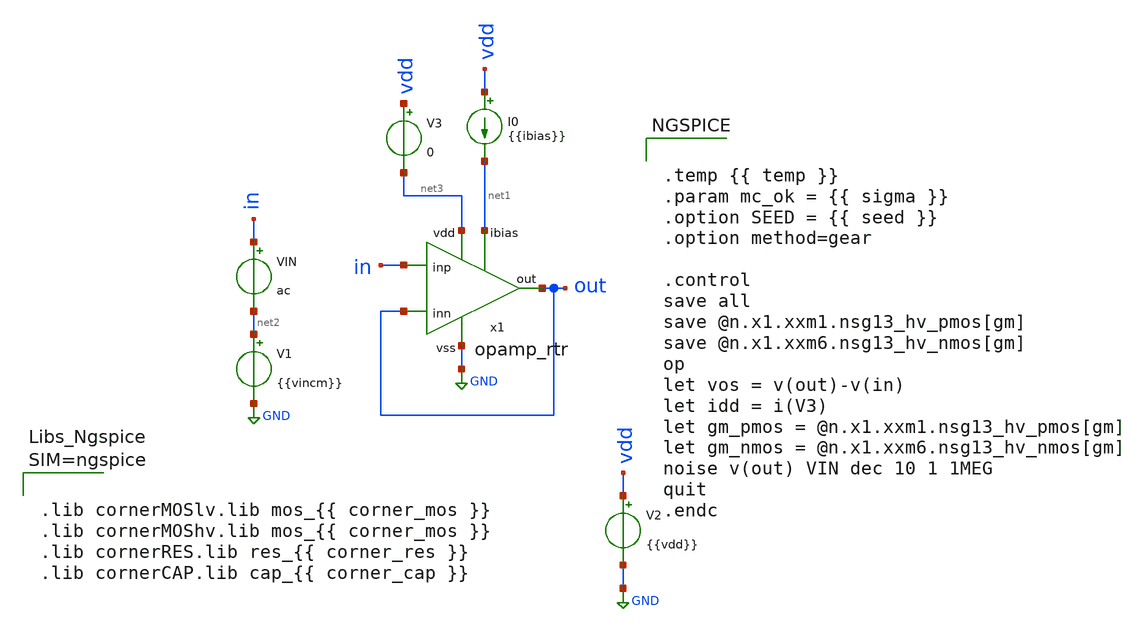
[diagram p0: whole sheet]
** sch_path: testbenches/xschem/tb_opamp_rtr_op.sch
**.subckt tb_opamp_rtr_op
V1 net2 GND {{vincm}}
.save i(v1)
V2 vdd GND {{vdd}}
I0 vdd net1 {{ibias}}
V3 vdd net3 0
.save i(v3)
VIN in net2 ac
.save i(vin)
x1 net3 in GND out net1 out opamp_rtr
**** begin user architecture code


.temp {{ temp }}
.param mc_ok = {{ sigma }}
.option SEED = {{ seed }}
.option method=gear

.control
save all
save @n.x1.xxm1.nsg13_hv_pmos[gm]
save @n.x1.xxm6.nsg13_hv_nmos[gm]
op
let vos = v(out)-v(in)
let idd = i(V3)
let gm_pmos = @n.x1.xxm1.nsg13_hv_pmos[gm]
let gm_nmos = @n.x1.xxm6.nsg13_hv_nmos[gm]
noise v(out) VIN dec 10 1 1MEG
quit
.endc





.lib cornerMOSlv.lib mos_{{ corner_mos }}
.lib cornerMOShv.lib mos_{{ corner_mos }}
.lib cornerRES.lib res_{{ corner_res }}
.lib cornerCAP.lib cap_{{ corner_cap }}



**** end user architecture code
**.ends

* expanding   symbol:  heichip/opamp_rtr/schematic/xschem/opamp_rtr.sym # of pins=6
** sym_path: schematic/xschem/opamp_rtr.sym
** sch_path: schematic/xschem/opamp_rtr.sch
.subckt opamp_rtr vdd inp vss inn ibias out
*.ipin inp
*.opin out
*.iopin vdd
*.ipin inn
*.ipin ibias
*.iopin vss
XXM6 out1_n inp ncmdiff_n vss sg13_hv_nmos w={w_diff_n} l={l_diff} ng={n_diff_n} m=1 mm_ok=1
XXM1 net1 inn ncmdiff_p vdd sg13_hv_pmos w={w_diff_p} l={l_diff} ng={n_diff_p} m=1 mm_ok=1
XXM2 ncmdiff_p inp out1_p vdd sg13_hv_pmos w={w_diff_p} l={l_diff} ng={n_diff_p} m=1 mm_ok=1
XXM3 ncmdiff_p vbias_p vdd vdd sg13_hv_pmos w={w_tail_p} l={l_bias} ng={n_tail_p} m=1 mm_ok=1
XXM4 vss net1 net1 vss sg13_hv_nmos w={w_load_n} l={l_load} ng={n_load_n} m=1 mm_ok=1
XXM5 out1_p net1 vss vss sg13_hv_nmos w={w_load_n} l={l_load} ng={n_load_n} m=1 mm_ok=1
XXM7 ncmdiff_n inn net2 vss sg13_hv_nmos w={w_diff_n} l={l_diff} ng={n_diff_n} m=1 mm_ok=1
XXM8 ncmdiff_n ibias vss vss sg13_hv_nmos w={w_tail_n} l={l_bias} ng={n_tail_n} m=1 mm_ok=1
XXM9 vdd net2 out1_n vdd sg13_hv_pmos w={w_load_p} l={l_load} ng={n_load_p} m=1 mm_ok=1
XXM10 net2 net2 vdd vdd sg13_hv_pmos w={w_load_p} l={l_load} ng={n_load_p} m=1 mm_ok=1
XXM25 nswa vref_p ncmdiff_p ncmdiff_p sg13_hv_pmos w={w_sw_p} l={l_sw} ng={n_sw_p} m=1 mm_ok=1
XXM26 nswa nswa vss vss sg13_hv_nmos w={w_gmn} l={l_bias} ng={n_gmn} m=1 mm_ok=1
XXM27 ncmdiff_n nswa vss vss sg13_hv_nmos w={w_gmn} l={l_bias} ng={n_gmn} m=1 mm_ok=1
XXM28 ncmdiff_n vref_n nswb vss sg13_hv_nmos w={w_sw_n} l={l_sw} ng={n_sw_n} m=1 mm_ok=1
XXM29 nswb nswb vdd vdd sg13_hv_pmos w={w_gmp} l={l_bias} ng={n_gmp} m=1 mm_ok=1
XXM30 ncmdiff_p nswb vdd vdd sg13_hv_pmos w={w_gmp} l={l_bias} ng={n_gmp} m=1 mm_ok=1
XXM13 out1_n nabn out1_p vss sg13_hv_nmos w={w_ab_n} l={l_ab} ng={n_ab_n} m=1 mm_ok=1
XXM14 out1_p nabp out1_n vdd sg13_hv_pmos w={w_ab_p} l={l_ab} ng={n_ab_p} m=1 mm_ok=1
XXM15 out1_n vbias_p vdd vdd sg13_hv_pmos w={w_ab_src} l={l_bias} ng={n_ab_src} m=1 mm_ok=1
XXM16 out1_p nab_ref vss vss sg13_hv_nmos w={w_ab_snk} l={l_bias} ng={n_ab_snk} m=1 mm_ok=1
XXM23 nab_ref vbias_p vdd vdd sg13_hv_pmos w={w_ab_src} l={l_bias} ng={n_ab_src} m=1 mm_ok=1
XXM24 nab_ref nab_ref vss vss sg13_hv_nmos w={w_ab_snk} l={l_bias} ng={n_ab_snk} m=1 mm_ok=1
XXM17 nabn vbias_p vdd vdd sg13_hv_pmos w={w_ab_src} l={l_bias} ng={n_ab_src} m=1 mm_ok=1
XXM18 nabn nabn net3 vss sg13_hv_nmos w={w_ab_n} l={l_ab} ng={n_ab_n} m=1 mm_ok=1
XXM19 net3 net3 vss vss sg13_hv_nmos w={w_ab_n} l={l_ab} ng={n_ab_n} m=1 mm_ok=1
XXM20 nabp nab_ref vss vss sg13_hv_nmos w={w_ab_snk} l={l_bias} ng={n_ab_snk} m=1 mm_ok=1
XXM21 nabp nabp net4 vdd sg13_hv_pmos w={w_ab_p} l={l_ab} ng={n_ab_p} m=1 mm_ok=1
XXM22 net4 net4 vdd vdd sg13_hv_pmos w={w_ab_p} l={l_ab} ng={n_ab_p} m=1 mm_ok=1
XXM11 out out1_n vdd vdd sg13_hv_pmos w={w_out_p} l={l_out} ng={n_out_p} m=1 mm_ok=1
XXM12 out out1_p vss vss sg13_hv_nmos w={w_out_n} l={l_out} ng={n_out_n} m=1 mm_ok=1
XXB1 ibias ibias vss vss sg13_hv_nmos w={w_bias_n} l={l_bias} ng={n_bias_n} m=1 mm_ok=1
XXB2 vbias_p ibias vss vss sg13_hv_nmos w={w_bias_n} l={l_bias} ng={n_bias_n} m=1 mm_ok=1
XXB5 vref_n vref_n vss vss sg13_hv_nmos w={w_ref_n} l={l_bias} ng={n_ref_n} m=1 mm_ok=1
XXB6 vref_p ibias vss vss sg13_hv_nmos w={w_bias_n} l={l_bias} ng={n_bias_n} m=1 mm_ok=1
XXB3 vbias_p vbias_p vdd vdd sg13_hv_pmos w={w_bias_p} l={l_bias} ng={n_bias_p} m=1 mm_ok=1
XXB4 vref_n vbias_p vdd vdd sg13_hv_pmos w={w_bias_p} l={l_bias} ng={n_bias_p} m=1 mm_ok=1
XXB7 vref_p vref_p vdd vdd sg13_hv_pmos w={w_ref_p} l={l_bias} ng={n_ref_p} m=1 mm_ok=1
**** begin user architecture code


*bias network
.param l_bias=4u
.param w_bias_p=15u
.param n_bias_p=4
.param w_bias_n=5u
.param n_bias_n=5
.param w_ref_n=5u
.param n_ref_n=4
.param w_ref_p=15u
.param n_ref_p=4
*first stage
.param l_diff=2u
.param l_load=4u

.param w_diff_n=5u
.param n_diff_n=4

.param w_diff_p=15u
.param n_diff_p=4

.param w_load_n=5u
.param n_load_n=4

.param w_load_p=15u
.param n_load_p=4

.param w_tail_n=5u
.param n_tail_n=4

.param w_tail_p=15u
.param n_tail_p=4

.param l_sw=1u
.param w_sw_p=15u
.param n_sw_p=4

.param w_sw_n=5u
.param n_sw_n=4

.param w_gmn=5u
.param n_gmn=4

.param w_gmp=15u
.param n_gmp=4

*output control circuit
.param w_ab_src=15u
.param n_ab_src=4
.param w_ab_snk=5u
.param n_ab_snk=4

.param w_ab_n=5u
.param n_ab_n=4
.param w_ab_p=15u
.param n_ab_p=4

.param l_ab=1u

.param w_out_p=60u
.param n_out_p=4
.param w_out_n=20u
.param n_out_n=4
.param l_out=1u

.param r_null=50k
.param c_null=500f



**** end user architecture code
XC3 out net5 cap_cmomf w=13.5e-6 l=21e-6 mmin=1 mmax=4 subblock=0 m=1 mm_ok=1
XC2 out net6 cap_cmomf w=13.5e-6 l=21e-6 mmin=1 mmax=4 subblock=0 m=1 mm_ok=1
XR4 net5 out1_n vss rhigh w=1e-6 l=36e-6 m=1 b=0 mm_ok=1
XR2 net6 out1_p vss rhigh w=1e-6 l=36e-6 m=1 b=0 mm_ok=1
XDUMMY1 ncmdiff_n ncmdiff_n ncmdiff_n vss sg13_hv_nmos w=5u l=0.45u ng=4 m=1 mm_ok=1
XDUMMY2 ncmdiff_n ncmdiff_n ncmdiff_n vss sg13_hv_nmos w=5u l=0.45u ng=2 m=1 mm_ok=1
XDUMMY3 vss vss vss vss sg13_hv_nmos w=7.5u l=0.45u ng=6 m=1 mm_ok=1
XDUMMY4 vss vss vss vss sg13_hv_nmos w=10u l=0.45u ng=4 m=1 mm_ok=1
XDUMMY5 out1_p out1_p out1_p vss sg13_hv_nmos w=5u l=1u ng=2 m=1 mm_ok=1
XDUMMY6 vdd vdd vdd vdd sg13_hv_pmos w=22.5u l=0.4u ng=6 m=1 mm_ok=1
XDUMMY7 nswa nswa nswa vdd sg13_hv_pmos w=15u l=0.4u ng=2 m=1 mm_ok=1
XDUMMY8 vdd vdd vdd vdd sg13_hv_pmos w=15u l=0.4u ng=4 m=1 mm_ok=1
XDUMMY9 vdd vdd vdd vdd sg13_hv_pmos w=37.5u l=0.4u ng=5 m=1 mm_ok=1
XDUMMY10 out1_n out1_n out1_n vdd sg13_hv_pmos w=15u l=0.4u ng=2 m=1 mm_ok=1
XDUMMY11 vss vss vss vss sg13_hv_nmos w=5u l=0.45u ng=2 m=1 mm_ok=1
XR3 vss vss vss rhigh w=1e-6 l=18e-6 m=1 b=0 mm_ok=1
.ends

.GLOBAL GND
.end
